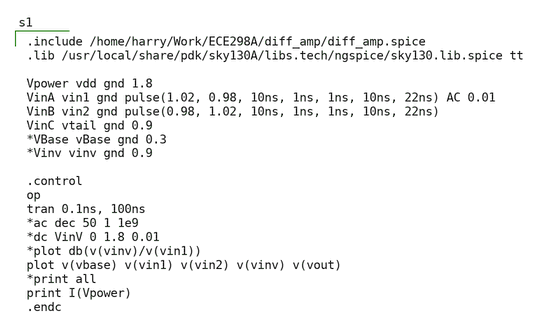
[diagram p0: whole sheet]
** sch_path: magic_xschem_ngspice/Magic_sim.sch
**.subckt Magic_sim
**** begin user architecture code

.include /home/harry/Work/ECE298A/diff_amp/diff_amp.spice
.lib /usr/local/share/pdk/sky130A/libs.tech/ngspice/sky130.lib.spice tt

Vpower vdd gnd 1.8
VinA vin1 gnd pulse(1.02, 0.98, 10ns, 1ns, 1ns, 10ns, 22ns) AC 0.01
VinB vin2 gnd pulse(0.98, 1.02, 10ns, 1ns, 1ns, 10ns, 22ns)
VinC vtail gnd 0.9
*VBase vBase gnd 0.3
*Vinv vinv gnd 0.9

.control
op
tran 0.1ns, 100ns
*ac dec 50 1 1e9
*dc VinV 0 1.8 0.01
*plot db(v(vinv)/v(vin1))
plot v(vbase) v(vin1) v(vin2) v(vinv) v(vout)
*print all
print I(Vpower)
.endc

**** end user architecture code
**.ends
.end
